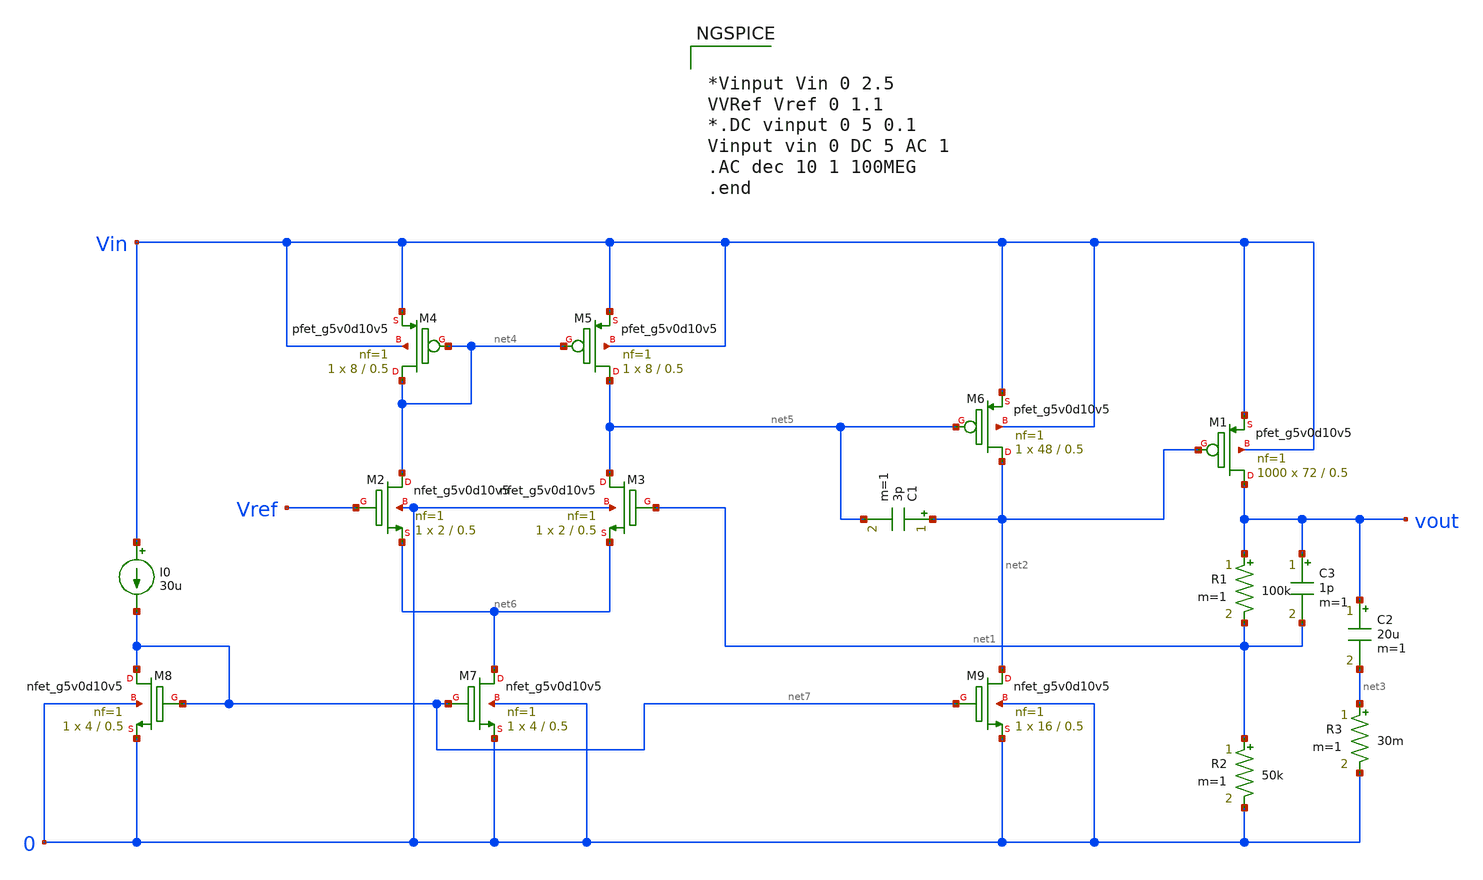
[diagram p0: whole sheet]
** sch_path: LDO/Schematic/LDO_Miller_OTA.sch
**.subckt LDO_Miller_OTA
R1 vout net1 100k m=1
R2 net1 0 50k m=1
XM1 vout net2 Vin Vin sky130_fd_pr__pfet_g5v0d10v5 L=0.5 W=72 nf=1 ad='int((nf+1)/2) * W/nf * 0.29' as='int((nf+2)/2) * W/nf * 0.29'
+ pd='2*int((nf+1)/2) * (W/nf + 0.29)' ps='2*int((nf+2)/2) * (W/nf + 0.29)' nrd='0.29 / W' nrs='0.29 / W'
+ sa=0 sb=0 sd=0 mult=1000 m=1000
C2 vout net3 20u m=1
R3 net3 0 30m m=1
C3 vout net1 1p m=1
C1 net2 net5 3p m=1
I0 Vin net7 30u
XM2 net4 Vref net6 0 sky130_fd_pr__nfet_g5v0d10v5 L=0.5 W=2 nf=1 ad='int((nf+1)/2) * W/nf * 0.29' as='int((nf+2)/2) * W/nf * 0.29'
+ pd='2*int((nf+1)/2) * (W/nf + 0.29)' ps='2*int((nf+2)/2) * (W/nf + 0.29)' nrd='0.29 / W' nrs='0.29 / W'
+ sa=0 sb=0 sd=0 mult=1 m=1
XM3 net5 net1 net6 0 sky130_fd_pr__nfet_g5v0d10v5 L=0.5 W=2 nf=1 ad='int((nf+1)/2) * W/nf * 0.29' as='int((nf+2)/2) * W/nf * 0.29'
+ pd='2*int((nf+1)/2) * (W/nf + 0.29)' ps='2*int((nf+2)/2) * (W/nf + 0.29)' nrd='0.29 / W' nrs='0.29 / W'
+ sa=0 sb=0 sd=0 mult=1 m=1
XM4 net4 net4 Vin Vin sky130_fd_pr__pfet_g5v0d10v5 L=0.5 W=8 nf=1 ad='int((nf+1)/2) * W/nf * 0.29' as='int((nf+2)/2) * W/nf * 0.29'
+ pd='2*int((nf+1)/2) * (W/nf + 0.29)' ps='2*int((nf+2)/2) * (W/nf + 0.29)' nrd='0.29 / W' nrs='0.29 / W'
+ sa=0 sb=0 sd=0 mult=1 m=1
XM5 net5 net4 Vin Vin sky130_fd_pr__pfet_g5v0d10v5 L=0.5 W=8 nf=1 ad='int((nf+1)/2) * W/nf * 0.29' as='int((nf+2)/2) * W/nf * 0.29'
+ pd='2*int((nf+1)/2) * (W/nf + 0.29)' ps='2*int((nf+2)/2) * (W/nf + 0.29)' nrd='0.29 / W' nrs='0.29 / W'
+ sa=0 sb=0 sd=0 mult=1 m=1
XM6 net2 net5 Vin Vin sky130_fd_pr__pfet_g5v0d10v5 L=0.5 W=48 nf=1 ad='int((nf+1)/2) * W/nf * 0.29' as='int((nf+2)/2) * W/nf * 0.29'
+ pd='2*int((nf+1)/2) * (W/nf + 0.29)' ps='2*int((nf+2)/2) * (W/nf + 0.29)' nrd='0.29 / W' nrs='0.29 / W'
+ sa=0 sb=0 sd=0 mult=1 m=1
XM7 net6 net7 0 0 sky130_fd_pr__nfet_g5v0d10v5 L=0.5 W=4 nf=1 ad='int((nf+1)/2) * W/nf * 0.29' as='int((nf+2)/2) * W/nf * 0.29'
+ pd='2*int((nf+1)/2) * (W/nf + 0.29)' ps='2*int((nf+2)/2) * (W/nf + 0.29)' nrd='0.29 / W' nrs='0.29 / W'
+ sa=0 sb=0 sd=0 mult=1 m=1
XM8 net7 net7 0 0 sky130_fd_pr__nfet_g5v0d10v5 L=0.5 W=4 nf=1 ad='int((nf+1)/2) * W/nf * 0.29' as='int((nf+2)/2) * W/nf * 0.29'
+ pd='2*int((nf+1)/2) * (W/nf + 0.29)' ps='2*int((nf+2)/2) * (W/nf + 0.29)' nrd='0.29 / W' nrs='0.29 / W'
+ sa=0 sb=0 sd=0 mult=1 m=1
XM9 net2 net7 0 0 sky130_fd_pr__nfet_g5v0d10v5 L=0.5 W=16 nf=1 ad='int((nf+1)/2) * W/nf * 0.29' as='int((nf+2)/2) * W/nf * 0.29'
+ pd='2*int((nf+1)/2) * (W/nf + 0.29)' ps='2*int((nf+2)/2) * (W/nf + 0.29)' nrd='0.29 / W' nrs='0.29 / W'
+ sa=0 sb=0 sd=0 mult=1 m=1
**** begin user architecture code


*Vinput Vin 0 2.5
VVRef Vref 0 1.1
*.DC vinput 0 5 0.1
Vinput vin 0 DC 5 AC 1
.AC dec 10 1 100MEG
.end



.include $::SKYWATER_MODELS/cells/nfet_01v8/sky130_fd_pr__nfet_01v8__tt.corner.spice
.include $::SKYWATER_MODELS/cells/nfet_01v8_lvt/sky130_fd_pr__nfet_01v8_lvt__tt.corner.spice
.include $::SKYWATER_MODELS/cells/pfet_01v8/sky130_fd_pr__pfet_01v8__tt.corner.spice
.include $::SKYWATER_MODELS/cells/nfet_03v3_nvt/sky130_fd_pr__nfet_03v3_nvt__tt.corner.spice
.include $::SKYWATER_MODELS/cells/nfet_05v0_nvt/sky130_fd_pr__nfet_05v0_nvt__tt.corner.spice
.include $::SKYWATER_MODELS/cells/esd_nfet_01v8/sky130_fd_pr__esd_nfet_01v8__tt.corner.spice
.include $::SKYWATER_MODELS/cells/pfet_01v8_lvt/sky130_fd_pr__pfet_01v8_lvt__tt.corner.spice
.include $::SKYWATER_MODELS/cells/pfet_01v8_hvt/sky130_fd_pr__pfet_01v8_hvt__tt.corner.spice
.include $::SKYWATER_MODELS/cells/esd_pfet_g5v0d10v5/sky130_fd_pr__esd_pfet_g5v0d10v5__tt.corner.spice
.include $::SKYWATER_MODELS/cells/pfet_g5v0d10v5/sky130_fd_pr__pfet_g5v0d10v5__tt.corner.spice
.include $::SKYWATER_MODELS/cells/pfet_g5v0d16v0/sky130_fd_pr__pfet_g5v0d16v0__tt.corner.spice
.include $::SKYWATER_MODELS/cells/nfet_g5v0d10v5/sky130_fd_pr__nfet_g5v0d10v5__tt.corner.spice
.include $::SKYWATER_MODELS/cells/nfet_g5v0d16v0/sky130_fd_pr__nfet_g5v0d16v0__tt_discrete.corner.spice
.include $::SKYWATER_MODELS/cells/esd_nfet_g5v0d10v5/sky130_fd_pr__esd_nfet_g5v0d10v5__tt.corner.spice
.include $::SKYWATER_MODELS/models/corners/tt/nonfet.spice
* Mismatch parameters
.include $::SKYWATER_MODELS/cells/nfet_01v8/sky130_fd_pr__nfet_01v8__mismatch.corner.spice
.include $::SKYWATER_MODELS/cells/pfet_01v8/sky130_fd_pr__pfet_01v8__mismatch.corner.spice
.include $::SKYWATER_MODELS/cells/nfet_01v8_lvt/sky130_fd_pr__nfet_01v8_lvt__mismatch.corner.spice
.include $::SKYWATER_MODELS/cells/pfet_01v8_lvt/sky130_fd_pr__pfet_01v8_lvt__mismatch.corner.spice
.include $::SKYWATER_MODELS/cells/pfet_01v8_hvt/sky130_fd_pr__pfet_01v8_hvt__mismatch.corner.spice
.include $::SKYWATER_MODELS/cells/nfet_g5v0d10v5/sky130_fd_pr__nfet_g5v0d10v5__mismatch.corner.spice
.include $::SKYWATER_MODELS/cells/pfet_g5v0d10v5/sky130_fd_pr__pfet_g5v0d10v5__mismatch.corner.spice
.include $::SKYWATER_MODELS/cells/nfet_05v0_nvt/sky130_fd_pr__nfet_05v0_nvt__mismatch.corner.spice
.include $::SKYWATER_MODELS/cells/nfet_03v3_nvt/sky130_fd_pr__nfet_03v3_nvt__mismatch.corner.spice
* Resistor$::SKYWATER_MODELS/Capacitor
.include $::SKYWATER_MODELS/models/r+c/res_typical__cap_typical.spice
.include $::SKYWATER_MODELS/models/r+c/res_typical__cap_typical__lin.spice
* Special cells
.include $::SKYWATER_MODELS/models/corners/tt/specialized_cells.spice
* All models
.include $::SKYWATER_MODELS/models/all.spice
* Corner
.include $::SKYWATER_MODELS/models/corners/tt/rf.spice

**** end user architecture code
**.ends
.end
